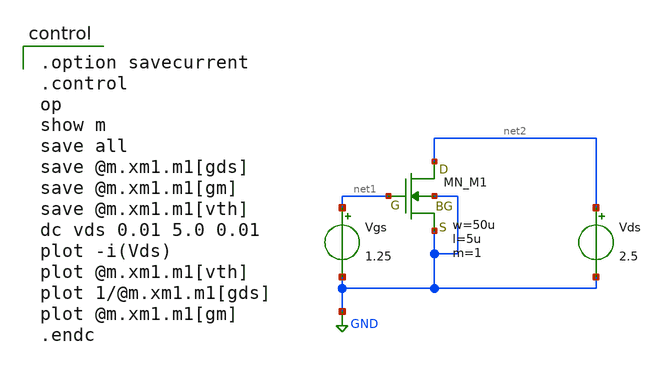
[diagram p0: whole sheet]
** sch_path: member_project/opamp/cat_nekonekone/meas_gm-rds-vth/nmos_idvds.sch
**.subckt nmos_idvds
Vgs net1 GND 1.25
Vds net2 GND 2.5
XM1 net2 net1 GND GND NMOS w=50u l=5u as=0 ad=0 ps=0 pd=0 nrd=0 nrs=0 m=1
**** begin user architecture code

.option savecurrent
.control
op
show m
save all
save @m.xm1.m1[gds]
save @m.xm1.m1[gm]
save @m.xm1.m1[vth]
dc vds 0.01 5.0 0.01
plot -i(Vds)
plot @m.xm1.m1[vth]
plot 1/@m.xm1.m1[gds]
plot @m.xm1.m1[gm]
.endc

 .include $::LIB/ip62_models
**** end user architecture code
**.ends
.GLOBAL GND
.end
